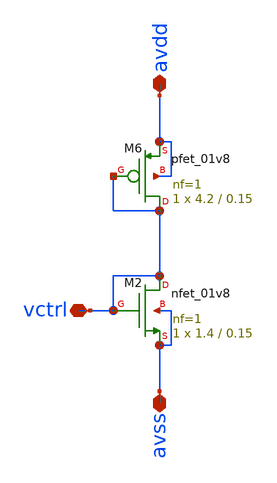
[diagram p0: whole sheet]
** sch_path: xschem/current_vc1.sch
**.subckt current_vc1 avdd avss vctrl
*.iopin avdd
*.iopin avss
*.iopin vctrl
XM2 vctrl vctrl avss avss sky130_fd_pr__nfet_01v8 L=0.15 W=1.4 nf=1 ad='int((nf+1)/2) * W/nf * 0.29'
+ as='int((nf+2)/2) * W/nf * 0.29' pd='2*int((nf+1)/2) * (W/nf + 0.29)' ps='2*int((nf+2)/2) * (W/nf + 0.29)'
+ nrd='0.29 / W' nrs='0.29 / W' sa=0 sb=0 sd=0 mult=1 m=1
XM6 vctrl vctrl avdd avdd sky130_fd_pr__pfet_01v8 L=0.15 W=4.2 nf=1 ad='int((nf+1)/2) * W/nf * 0.29'
+ as='int((nf+2)/2) * W/nf * 0.29' pd='2*int((nf+1)/2) * (W/nf + 0.29)' ps='2*int((nf+2)/2) * (W/nf + 0.29)'
+ nrd='0.29 / W' nrs='0.29 / W' sa=0 sb=0 sd=0 mult=1 m=1
**.ends
.end
